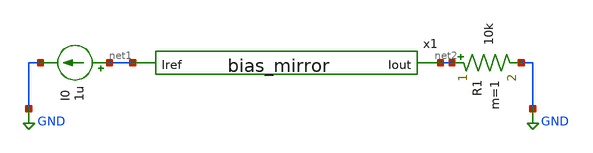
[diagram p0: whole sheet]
** sch_path: bias_mirror/sim/tb_bias_mirror.sch
**.subckt tb_bias_mirror
x1 net2 net1 bias_mirror
I0 net1 GND 1u
R1 net2 GND 10k m=1
**** begin user architecture code



.lib /foss/pdks/sky130A/libs.tech/ngspice/sky130.lib.spice tt
.dc I0 1u 20u 1u
.save all

**** end user architecture code
**.ends

* expanding   symbol:  /headless/pulse-generator/bias_mirror/bias_mirror.sym # of pins=2
** sym_path: bias_mirror/bias_mirror.sym
** sch_path: bias_mirror/bias_mirror.sch
.subckt bias_mirror Iout Iref
*.ipin Iref
*.opin Iout
XM1 Iout Iref VDD VDD sky130_fd_pr__pfet_01v8 L=0.5 W=2 nf=1 ad='int((1 + 1)/2) * 2 / 1 * 0.29' as='int((1 + 2)/2) * 2 / 1 * 0.29'
+ pd='2*int((1 + 1)/2) * (2 / 1 + 0.29)' ps='2*int((1 + 2)/2) * (2 / 1 + 0.29)' nrd='0.29 / 2 ' nrs='0.29 / 2 '
+ sa=0 sb=0 sd=0 mult=1 m=1
XM2 Iref Iref VDD VDD sky130_fd_pr__pfet_01v8 L=0.5 W=2 nf=1 ad='int((1 + 1)/2) * 2 / 1 * 0.29' as='int((1 + 2)/2) * 2 / 1 * 0.29'
+ pd='2*int((1 + 1)/2) * (2 / 1 + 0.29)' ps='2*int((1 + 2)/2) * (2 / 1 + 0.29)' nrd='0.29 / 2 ' nrs='0.29 / 2 '
+ sa=0 sb=0 sd=0 mult=1 m=1
V1 VDD GND 1.8
.ends

.GLOBAL GND
.end
